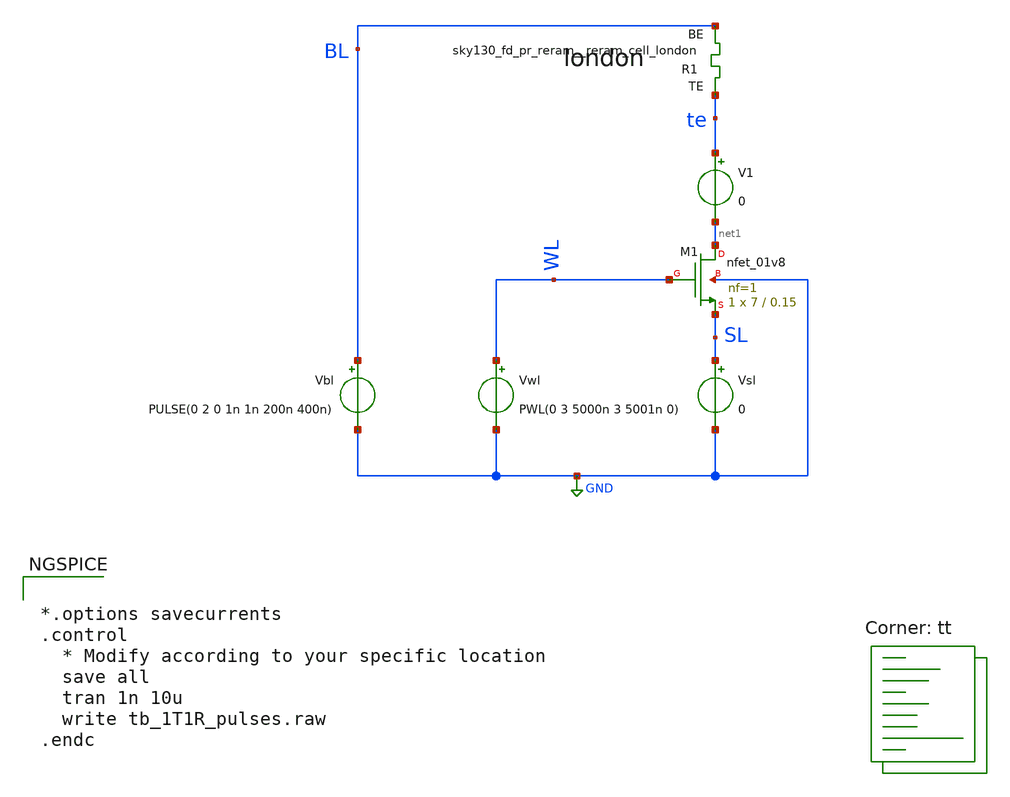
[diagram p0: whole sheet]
** sch_path: memristor_models/rram_london/tb_1T1R_pulses.sch
**.subckt tb_1T1R_pulses
XM1 net1 WL SL GND sky130_fd_pr__nfet_01v8 L=0.15 W=7 nf=1 ad='int((nf+1)/2) * W/nf * 0.29' as='int((nf+2)/2) * W/nf * 0.29'
+ pd='2*int((nf+1)/2) * (W/nf + 0.29)' ps='2*int((nf+2)/2) * (W/nf + 0.29)' nrd='0.29 / W' nrs='0.29 / W'
+ sa=0 sb=0 sd=0 mult=1 m=1
Vwl WL GND PWL(0 3 5000n 3 5001n 0)
Vbl BL GND PULSE(0 2 0 1n 1n 200n 400n)
V1 te net1 0
Vsl SL GND 0
XR1 te BL sky130_fd_pr_reram__reram_cell_london
**** begin user architecture code


*.options savecurrents
.control
  * Modify according to your specific location
  save all
  tran 1n 10u
  write tb_1T1R_pulses.raw
.endc



.lib $::SKYWATER_MODELS/sky130.lib.spice tt

** opencircuitdesign pdks install
.inc $::SKYWATER_MODELS/sky130_fd_pr_reram__reram_cell_london.spice

**** end user architecture code
**.ends
.GLOBAL GND
.end
